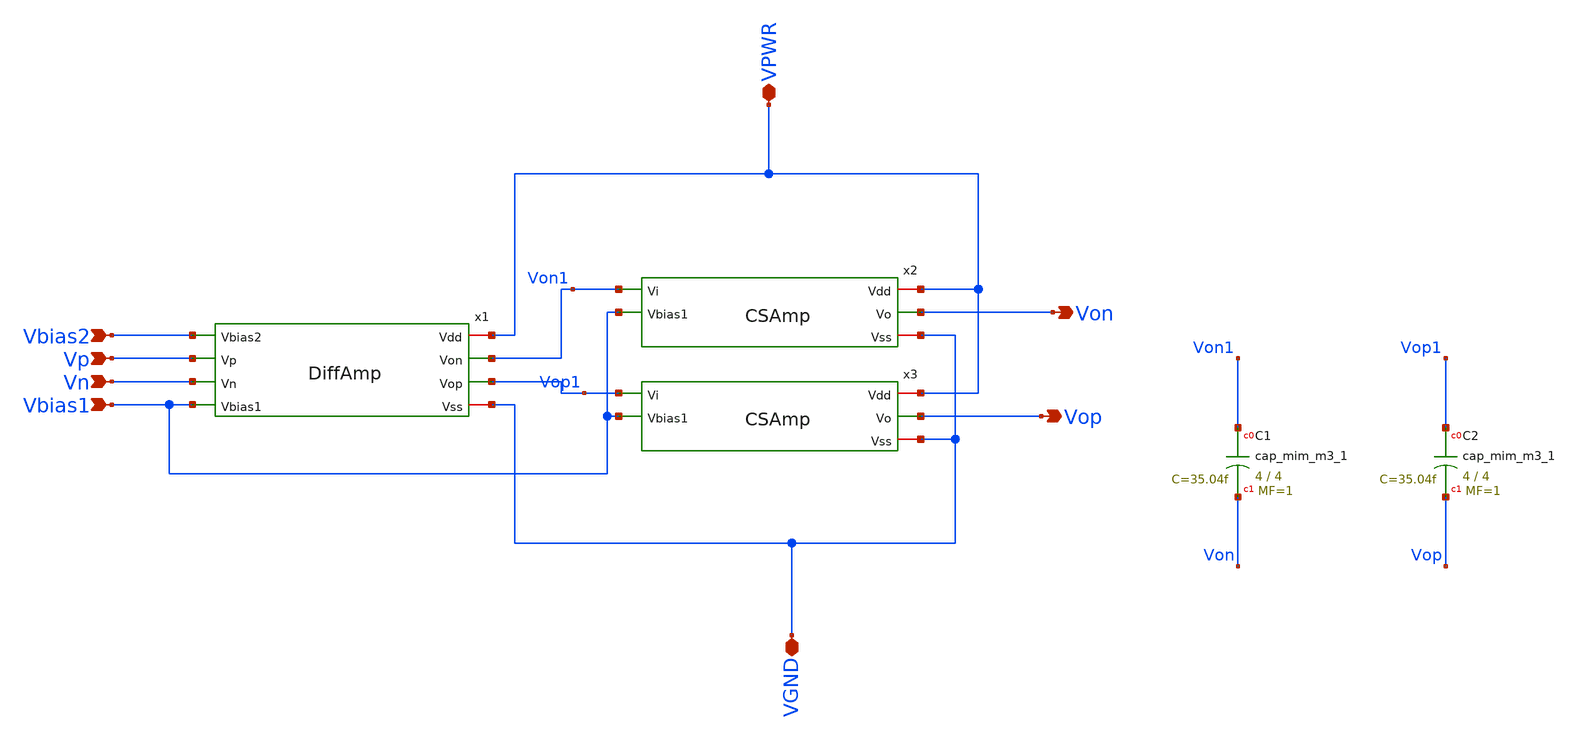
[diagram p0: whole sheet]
** sch_path: Circuits/MillerOpAmpCMMFB/MillerOpAmp.sch
**.subckt MillerOpAmp Von Vop Vbias2 Vp Vn Vbias1 VPWR VGND
*.opin Von
*.opin Vop
*.ipin Vbias2
*.ipin Vp
*.ipin Vn
*.ipin Vbias1
*.iopin VPWR
*.iopin VGND
XC1 Von1 Von sky130_fd_pr__cap_mim_m3_1 W=4 L=4 MF=1 m=1
XC2 Vop1 Vop sky130_fd_pr__cap_mim_m3_1 W=4 L=4 MF=1 m=1
x1 VPWR Vbias2 Von1 Vop1 Vp Vn Vbias1 VGND DiffAmp
x2 VPWR Von1 Von Vbias1 VGND CSAmp
x3 VPWR Vop1 Vop Vbias1 VGND CSAmp
**.ends
.end
